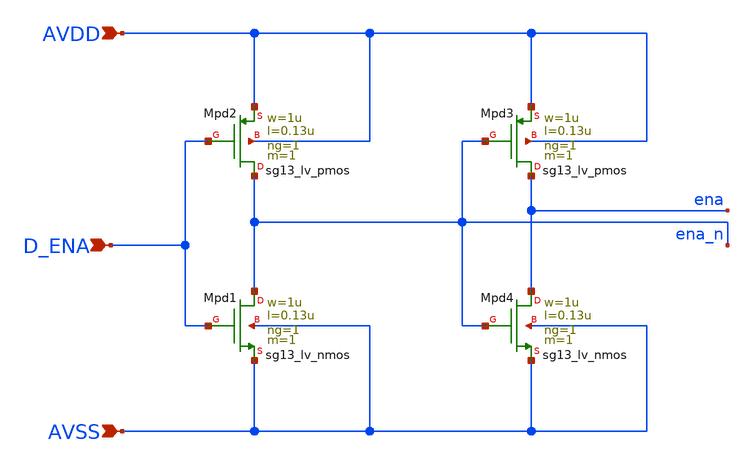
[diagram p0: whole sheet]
** sch_path: Designs/otas/1_schematics/enable_pins.sch
**.subckt enable_pins AVSS AVDD D_ENA
*.ipin AVSS
*.ipin AVDD
*.ipin D_ENA
XMpd2 ena_n D_ENA AVDD AVDD sg13_lv_pmos w=1u l=0.13u ng=1 m=1 mm_ok=1
XMpd3 ena ena_n AVDD AVDD sg13_lv_pmos w=1u l=0.13u ng=1 m=1 mm_ok=1
XMpd1 ena_n D_ENA AVSS AVSS sg13_lv_nmos w=1u l=0.13u ng=1 m=1 mm_ok=1
XMpd4 ena ena_n AVSS AVSS sg13_lv_nmos w=1u l=0.13u ng=1 m=1 mm_ok=1
**.ends
.end
